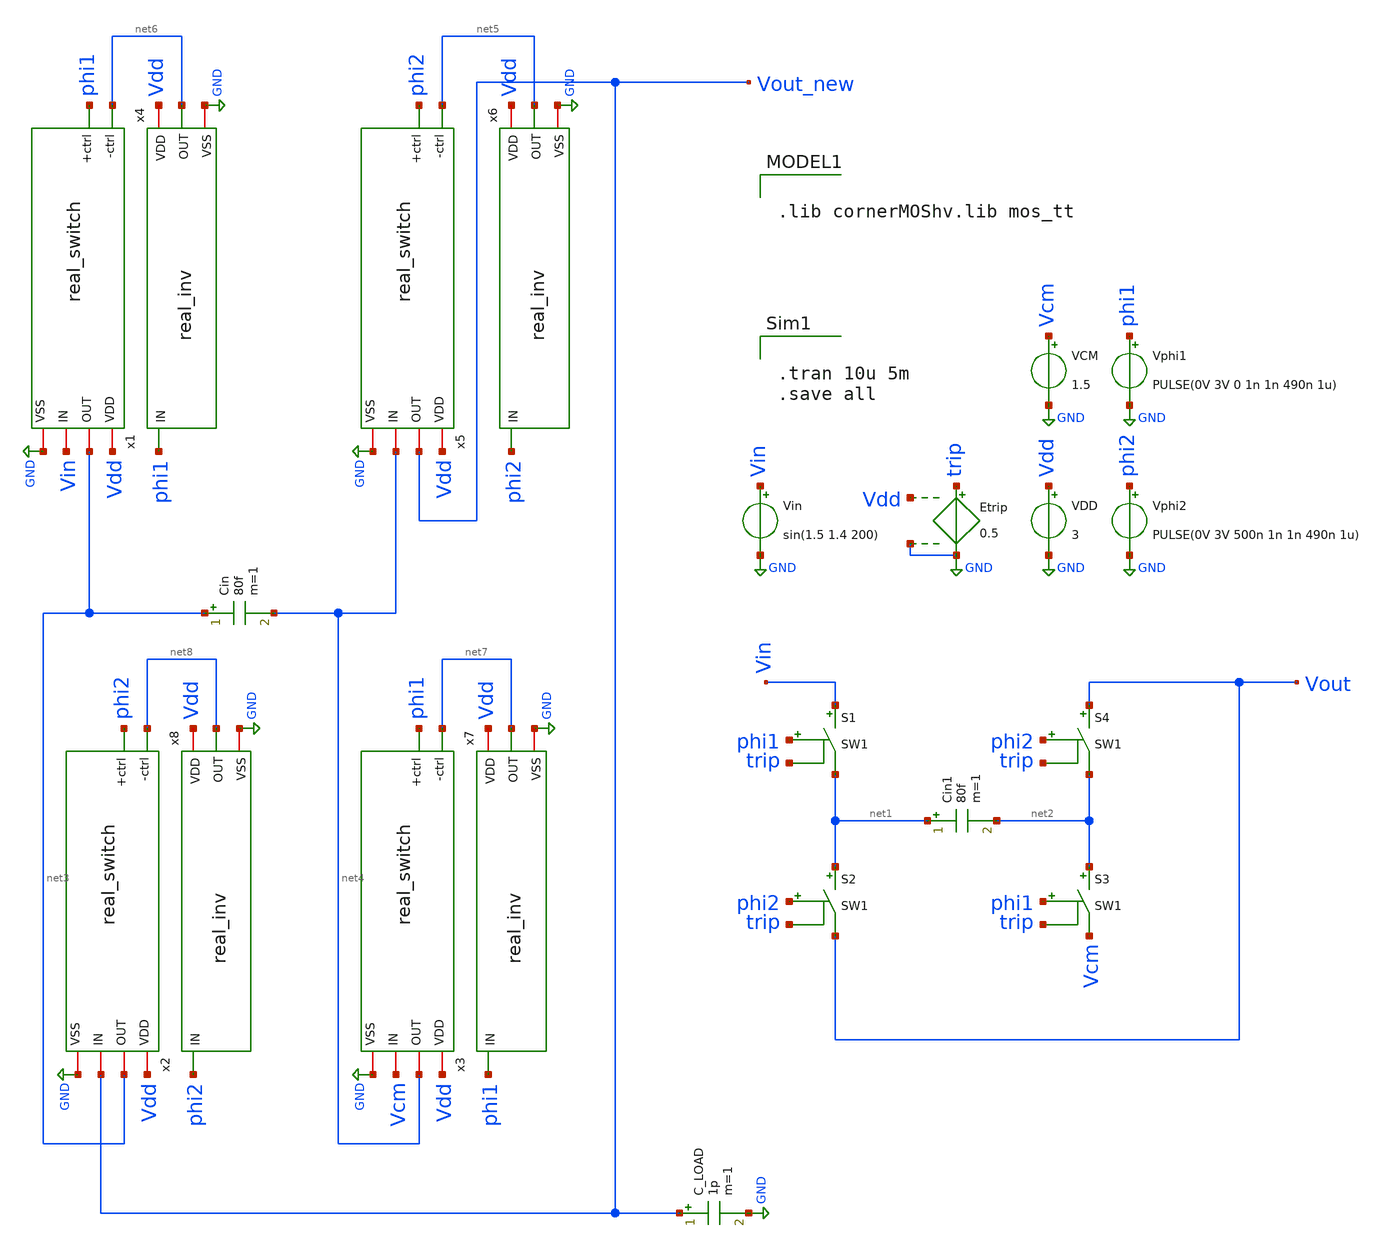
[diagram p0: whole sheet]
** sch_path: real_circuit/sandbox/real_switches.sch
**.subckt real_switches
S2 net1 Vout phi2 trip SW1
S1 Vin net1 phi1 trip SW1
S3 net2 Vcm phi1 trip SW1
S4 Vout net2 phi2 trip SW1
Cin net3 net4 80f m=1
Cin1 net1 net2 80f m=1
Etrip trip GND Vdd GND 0.5
VDD Vdd GND 3
VCM Vcm GND 1.5
Vin Vin GND sin(1.5 1.4 200)
Vphi1 phi1 GND PULSE(0V 3V 0 1n 1n 490n 1u)
Vphi2 phi2 GND PULSE(0V 3V 500n 1n 1n 490n 1u)
x1 net6 Vdd net3 Vin phi1 GND real_switch
x5 net5 Vdd Vout_new net4 phi2 GND real_switch
x2 net8 Vdd net3 Vout_new phi2 GND real_switch
x3 net7 Vdd net4 Vcm phi1 GND real_switch
C_LOAD Vout_new GND 1p m=1
x4 Vdd phi1 net6 GND real_inv
x6 Vdd phi2 net5 GND real_inv
x7 Vdd phi1 net7 GND real_inv
x8 Vdd phi2 net8 GND real_inv
**** begin user architecture code


.tran 10u 5m
.save all



.lib cornerMOShv.lib mos_tt

**** end user architecture code
**.ends

* expanding   symbol:  /foss/designs/real/real_switch.sym # of pins=6
** sym_path: real_circuit/sandbox/real_switch.sym
** sch_path: real_circuit/sandbox/real_switch.sch
.subckt real_switch -ctrl VDD OUT IN +ctrl VSS
*.iopin IN
*.iopin OUT
*.iopin VDD
*.iopin VSS
*.ipin +ctrl
*.ipin -ctrl
XM1 OUT -ctrl IN VSS sg13_hv_nmos w=1u l=0.6u ng=1 m=1 mm_ok=1
XM2 OUT +ctrl IN VDD sg13_hv_pmos w=2.5u l=0.6u ng=1 m=1 mm_ok=1
.ends


* expanding   symbol:  /foss/designs/real/real_inv.sym # of pins=4
** sym_path: real_circuit/real_inv.sym
** sch_path: real_circuit/real_inv.sch
.subckt real_inv VDD IN OUT VSS
*.iopin VDD
*.iopin VSS
*.ipin IN
*.opin OUT
XM1 OUT IN VDD VDD sg13_hv_pmos w=0.6u l=0.4u ng=1 m=1 mm_ok=1
XM2 OUT IN VSS VSS sg13_hv_nmos w=0.3u l=0.45u ng=1 m=1 mm_ok=1
.ends

.GLOBAL GND
**** begin user architecture code
.MODEL SW1 SW   VT=0.9 VH=0.01  RON=0.1 ROFF=10G
**** end user architecture code
.end
